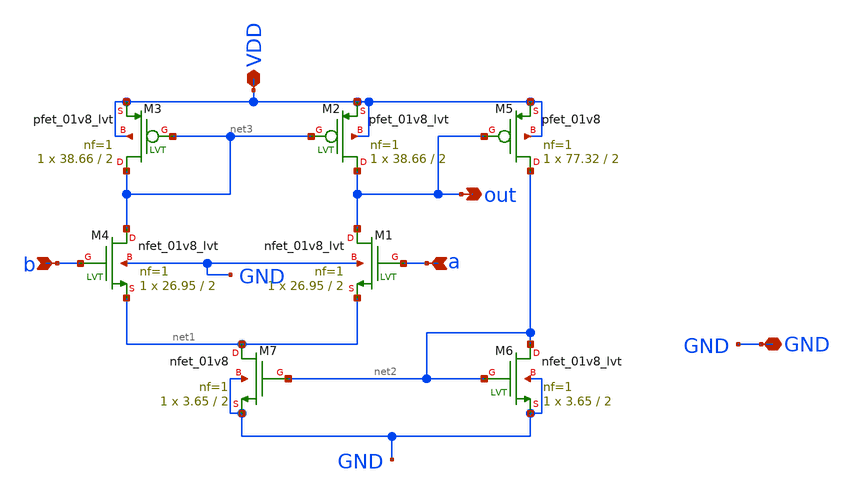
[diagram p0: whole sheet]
** sch_path: schematic/amplifier_self_bias.sch
**.subckt amplifier_self_bias b a VDD out GND
*.ipin b
*.ipin a
*.iopin VDD
*.opin out
*.iopin GND
XM1 out a net1 GND sky130_fd_pr__nfet_01v8_lvt L=2 W=26.95 nf=1 ad='int((nf+1)/2) * W/nf * 0.29' as='int((nf+2)/2) * W/nf * 0.29'
+ pd='2*int((nf+1)/2) * (W/nf + 0.29)' ps='2*int((nf+2)/2) * (W/nf + 0.29)' nrd='0.29 / W' nrs='0.29 / W'
+ sa=0 sb=0 sd=0 mult=1 m=1
XM2 out net3 VDD VDD sky130_fd_pr__pfet_01v8_lvt L=2 W=38.66 nf=1 ad='int((nf+1)/2) * W/nf * 0.29' as='int((nf+2)/2) * W/nf * 0.29'
+ pd='2*int((nf+1)/2) * (W/nf + 0.29)' ps='2*int((nf+2)/2) * (W/nf + 0.29)' nrd='0.29 / W' nrs='0.29 / W'
+ sa=0 sb=0 sd=0 mult=1 m=1
XM3 net3 net3 VDD VDD sky130_fd_pr__pfet_01v8_lvt L=2 W=38.66 nf=1 ad='int((nf+1)/2) * W/nf * 0.29' as='int((nf+2)/2) * W/nf * 0.29'
+ pd='2*int((nf+1)/2) * (W/nf + 0.29)' ps='2*int((nf+2)/2) * (W/nf + 0.29)' nrd='0.29 / W' nrs='0.29 / W'
+ sa=0 sb=0 sd=0 mult=1 m=1
XM4 net3 b net1 GND sky130_fd_pr__nfet_01v8_lvt L=2 W=26.95 nf=1 ad='int((nf+1)/2) * W/nf * 0.29' as='int((nf+2)/2) * W/nf * 0.29'
+ pd='2*int((nf+1)/2) * (W/nf + 0.29)' ps='2*int((nf+2)/2) * (W/nf + 0.29)' nrd='0.29 / W' nrs='0.29 / W'
+ sa=0 sb=0 sd=0 mult=1 m=1
XM5 net2 out VDD VDD sky130_fd_pr__pfet_01v8 L=2 W=77.32 nf=1 ad='int((nf+1)/2) * W/nf * 0.29' as='int((nf+2)/2) * W/nf * 0.29'
+ pd='2*int((nf+1)/2) * (W/nf + 0.29)' ps='2*int((nf+2)/2) * (W/nf + 0.29)' nrd='0.29 / W' nrs='0.29 / W'
+ sa=0 sb=0 sd=0 mult=1 m=1
XM6 net2 net2 GND GND sky130_fd_pr__nfet_01v8_lvt L=2 W=3.65 nf=1 ad='int((nf+1)/2) * W/nf * 0.29' as='int((nf+2)/2) * W/nf * 0.29'
+ pd='2*int((nf+1)/2) * (W/nf + 0.29)' ps='2*int((nf+2)/2) * (W/nf + 0.29)' nrd='0.29 / W' nrs='0.29 / W'
+ sa=0 sb=0 sd=0 mult=1 m=1
XM7 net1 net2 GND GND sky130_fd_pr__nfet_01v8 L=2 W=3.65 nf=1 ad='int((nf+1)/2) * W/nf * 0.29' as='int((nf+2)/2) * W/nf * 0.29'
+ pd='2*int((nf+1)/2) * (W/nf + 0.29)' ps='2*int((nf+2)/2) * (W/nf + 0.29)' nrd='0.29 / W' nrs='0.29 / W'
+ sa=0 sb=0 sd=0 mult=1 m=1
**.ends
.end
